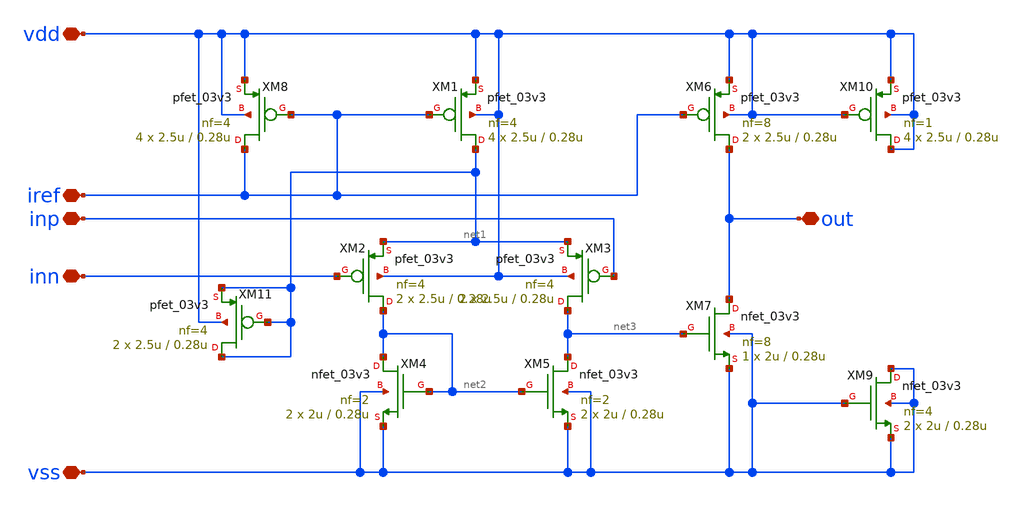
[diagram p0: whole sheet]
** sch_path: designs/libs/qw_core_analog/Pcomparator/Pcomparator.sch
**.subckt Pcomparator inp inn vdd vss out iref
*.iopin inp
*.iopin inn
*.iopin vdd
*.iopin vss
*.iopin out
*.iopin iref
XM8 iref iref vdd vdd pfet_03v3 L=0.28u W=2.5u nf=4 ad='int((nf+1)/2) * W/nf * 0.18u' as='int((nf+2)/2) * W/nf * 0.18u'
+ pd='2*int((nf+1)/2) * (W/nf + 0.18u)' ps='2*int((nf+2)/2) * (W/nf + 0.18u)' nrd='0.18u / W' nrs='0.18u / W'
+ sa=0 sb=0 sd=0 m=4
XM1 net1 iref vdd vdd pfet_03v3 L=0.28u W=2.5u nf=4 ad='int((nf+1)/2) * W/nf * 0.18u' as='int((nf+2)/2) * W/nf * 0.18u'
+ pd='2*int((nf+1)/2) * (W/nf + 0.18u)' ps='2*int((nf+2)/2) * (W/nf + 0.18u)' nrd='0.18u / W' nrs='0.18u / W'
+ sa=0 sb=0 sd=0 m=4
XM2 net2 inn net1 vdd pfet_03v3 L=0.28u W=2.5u nf=4 ad='int((nf+1)/2) * W/nf * 0.18u' as='int((nf+2)/2) * W/nf * 0.18u'
+ pd='2*int((nf+1)/2) * (W/nf + 0.18u)' ps='2*int((nf+2)/2) * (W/nf + 0.18u)' nrd='0.18u / W' nrs='0.18u / W'
+ sa=0 sb=0 sd=0 m=2
XM3 net3 inp net1 vdd pfet_03v3 L=0.28u W=2.5u nf=4 ad='int((nf+1)/2) * W/nf * 0.18u' as='int((nf+2)/2) * W/nf * 0.18u'
+ pd='2*int((nf+1)/2) * (W/nf + 0.18u)' ps='2*int((nf+2)/2) * (W/nf + 0.18u)' nrd='0.18u / W' nrs='0.18u / W'
+ sa=0 sb=0 sd=0 m=2
XM4 net2 net2 vss vss nfet_03v3 L=0.28u W=2u nf=2 ad='int((nf+1)/2) * W/nf * 0.18u' as='int((nf+2)/2) * W/nf * 0.18u'
+ pd='2*int((nf+1)/2) * (W/nf + 0.18u)' ps='2*int((nf+2)/2) * (W/nf + 0.18u)' nrd='0.18u / W' nrs='0.18u / W'
+ sa=0 sb=0 sd=0 m=2
XM5 net3 net2 vss vss nfet_03v3 L=0.28u W=2u nf=2 ad='int((nf+1)/2) * W/nf * 0.18u' as='int((nf+2)/2) * W/nf * 0.18u'
+ pd='2*int((nf+1)/2) * (W/nf + 0.18u)' ps='2*int((nf+2)/2) * (W/nf + 0.18u)' nrd='0.18u / W' nrs='0.18u / W'
+ sa=0 sb=0 sd=0 m=2
XM6 out iref vdd vdd pfet_03v3 L=0.28u W=2.5u nf=8 ad='int((nf+1)/2) * W/nf * 0.18u' as='int((nf+2)/2) * W/nf * 0.18u'
+ pd='2*int((nf+1)/2) * (W/nf + 0.18u)' ps='2*int((nf+2)/2) * (W/nf + 0.18u)' nrd='0.18u / W' nrs='0.18u / W'
+ sa=0 sb=0 sd=0 m=2
XM7 out net3 vss vss nfet_03v3 L=0.28u W=2u nf=8 ad='int((nf+1)/2) * W/nf * 0.18u' as='int((nf+2)/2) * W/nf * 0.18u'
+ pd='2*int((nf+1)/2) * (W/nf + 0.18u)' ps='2*int((nf+2)/2) * (W/nf + 0.18u)' nrd='0.18u / W' nrs='0.18u / W'
+ sa=0 sb=0 sd=0 m=1
XM9 vss vss vss vss nfet_03v3 L=0.28u W=2u nf=4 ad='int((nf+1)/2) * W/nf * 0.18u' as='int((nf+2)/2) * W/nf * 0.18u'
+ pd='2*int((nf+1)/2) * (W/nf + 0.18u)' ps='2*int((nf+2)/2) * (W/nf + 0.18u)' nrd='0.18u / W' nrs='0.18u / W'
+ sa=0 sb=0 sd=0 m=2
XM10 vdd vdd vdd vdd pfet_03v3 L=0.28u W=2.5u nf=1 ad='int((nf+1)/2) * W/nf * 0.18u' as='int((nf+2)/2) * W/nf * 0.18u'
+ pd='2*int((nf+1)/2) * (W/nf + 0.18u)' ps='2*int((nf+2)/2) * (W/nf + 0.18u)' nrd='0.18u / W' nrs='0.18u / W'
+ sa=0 sb=0 sd=0 m=4
XM11 net1 net1 net1 vdd pfet_03v3 L=0.28u W=2.5u nf=4 ad='int((nf+1)/2) * W/nf * 0.18u' as='int((nf+2)/2) * W/nf * 0.18u'
+ pd='2*int((nf+1)/2) * (W/nf + 0.18u)' ps='2*int((nf+2)/2) * (W/nf + 0.18u)' nrd='0.18u / W' nrs='0.18u / W'
+ sa=0 sb=0 sd=0 m=2
**.ends
.end
